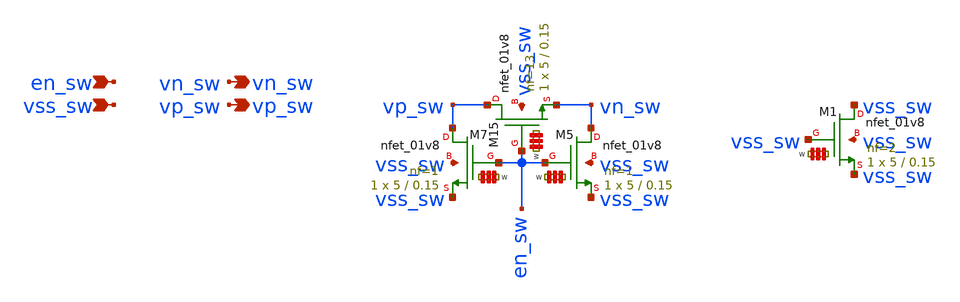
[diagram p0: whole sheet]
** sch_path: cap_sw.sch
**.subckt cap_sw en_sw vss_sw vn_sw vp_sw
*.ipin en_sw
*.ipin vss_sw
*.opin vn_sw
*.opin vp_sw
XM15 vp_sw en_sw vn_sw vss_sw sky130_fd_pr__nfet_01v8 L=0.15 W='5 * 13 ' nf=13 ad='int((nf+1)/2) * W / nf * 0.29'
+ as='int((nf+2)/2) * W / nf * 0.29' pd='2*int((nf+1)/2) * (W / nf + 0.29)' ps='2*int((nf+2)/2) * (W / nf + 0.29)'
+ nrd='0.29 / W ' nrs='0.29 / W ' sa=0 sb=0 sd=0 mult=1 m=1
XM5 vn_sw en_sw vss_sw vss_sw sky130_fd_pr__nfet_01v8 L=0.15 W='5 * 1 ' nf=1 ad='int((nf+1)/2) * W / nf * 0.29'
+ as='int((nf+2)/2) * W / nf * 0.29' pd='2*int((nf+1)/2) * (W / nf + 0.29)' ps='2*int((nf+2)/2) * (W / nf + 0.29)'
+ nrd='0.29 / W ' nrs='0.29 / W ' sa=0 sb=0 sd=0 mult=1 m=1
XM7 vp_sw en_sw vss_sw vss_sw sky130_fd_pr__nfet_01v8 L=0.15 W='5 * 1 ' nf=1 ad='int((nf+1)/2) * W / nf * 0.29'
+ as='int((nf+2)/2) * W / nf * 0.29' pd='2*int((nf+1)/2) * (W / nf + 0.29)' ps='2*int((nf+2)/2) * (W / nf + 0.29)'
+ nrd='0.29 / W ' nrs='0.29 / W ' sa=0 sb=0 sd=0 mult=1 m=1
XM1 vss_sw vss_sw vss_sw vss_sw sky130_fd_pr__nfet_01v8 L=0.15 W='5 * 2 ' nf=2 ad='int((nf+1)/2) * W / nf * 0.29'
+ as='int((nf+2)/2) * W / nf * 0.29' pd='2*int((nf+1)/2) * (W / nf + 0.29)' ps='2*int((nf+2)/2) * (W / nf + 0.29)'
+ nrd='0.29 / W ' nrs='0.29 / W ' sa=0 sb=0 sd=0 mult=1 m=1
**.ends
.end
